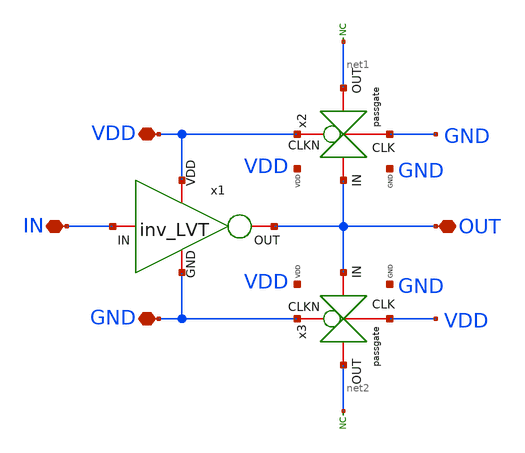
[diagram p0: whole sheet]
** sch_path: LVT/rovcel2_LVT/rovcel2_LVT.sch
**.subckt rovcel2_LVT OUT IN VDD GND
*.iopin OUT
*.iopin IN
*.iopin VDD
*.iopin GND
* noconn #net1
* noconn #net2
x1 VDD IN OUT GND inv_LVT
x2 VDD OUT net1 GND GND VDD passgate
x3 GND OUT net2 VDD GND VDD passgate
**.ends
.GLOBAL VDD
.GLOBAL GND
.end
